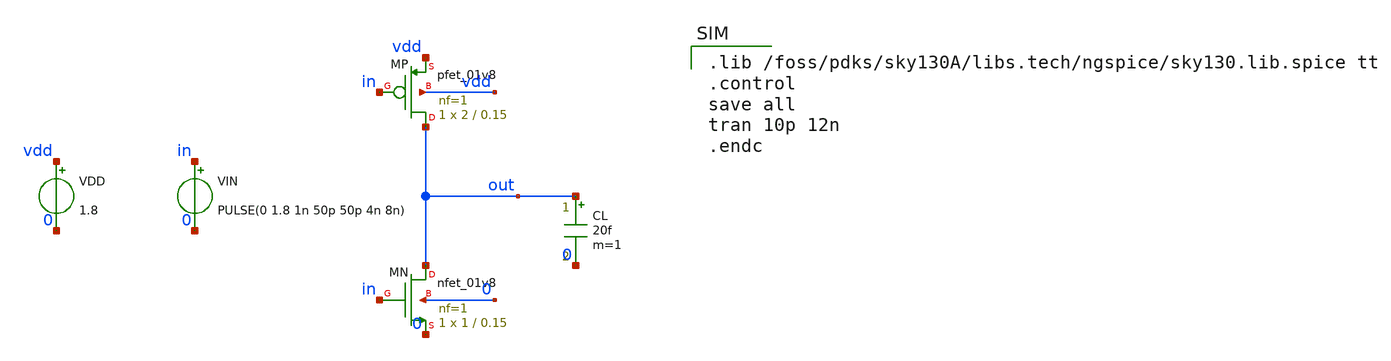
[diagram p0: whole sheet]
** sch_path: examples/sky130-simulation/inverter.sch
**.subckt inverter
VDD vdd 0 1.8
VIN in 0 PULSE(0 1.8 1n 50p 50p 4n 8n)
XMP out in vdd vdd sky130_fd_pr__pfet_01v8 L=0.15 W=2 nf=1 ad='int((nf+1)/2) * W/nf * 0.29' as='int((nf+2)/2) * W/nf * 0.29'
+ pd='2*int((nf+1)/2) * (W/nf + 0.29)' ps='2*int((nf+2)/2) * (W/nf + 0.29)' nrd='0.29 / W' nrs='0.29 / W'
+ sa=0 sb=0 sd=0 mult=1 m=1
XMN out in 0 0 sky130_fd_pr__nfet_01v8 L=0.15 W=1 nf=1 ad='int((1 + 1)/2) * 1 / 1 * 0.29' as='int((1 + 2)/2) * 1 / 1 * 0.29'
+ pd='2*int((1 + 1)/2) * (1 / 1 + 0.29)' ps='2*int((1 + 2)/2) * (1 / 1 + 0.29)' nrd='0.29 / 1 ' nrs='0.29 / 1 '
+ sa=0 sb=0 sd=0 mult=1 m=1
CL out 0 20f m=1
**** begin user architecture code

.lib /foss/pdks/sky130A/libs.tech/ngspice/sky130.lib.spice tt
.control
save all
tran 10p 12n
.endc

**** end user architecture code
**.ends
.end
